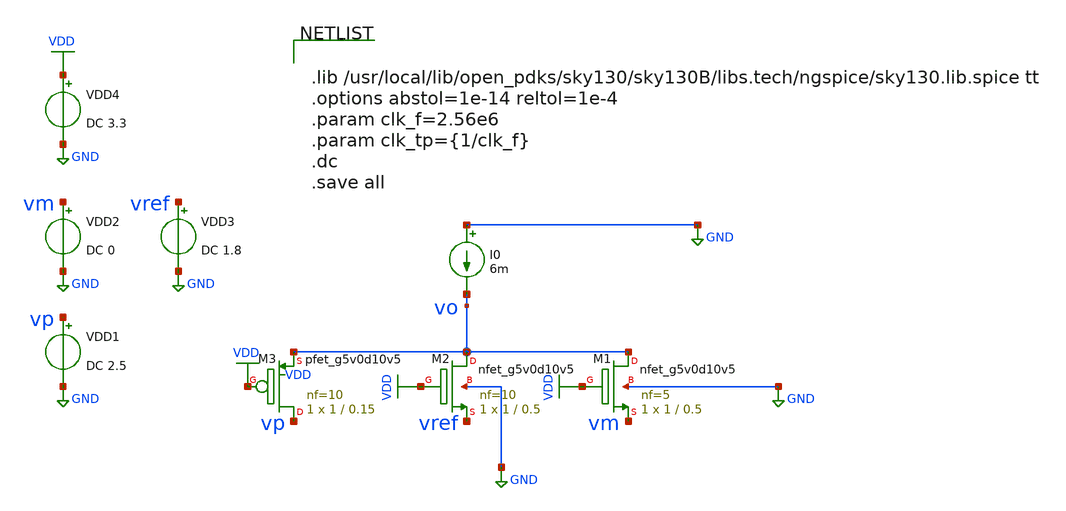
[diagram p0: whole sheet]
** sch_path: xschem/tryandtest/tb_fingers.sch
**.subckt tb_fingers
VDD4 VDD GND DC 3.3
VDD1 vp GND DC 2.5
VDD2 vm GND DC 0
VDD3 vref GND DC 1.8
I0 GND vo 6m
XM1 vo VDD vm GND sky130_fd_pr__nfet_g5v0d10v5 L=0.5 W=1 nf=5 ad='int((nf+1)/2) * W/nf * 0.29' as='int((nf+2)/2) * W/nf * 0.29'
+ pd='2*int((nf+1)/2) * (W/nf + 0.29)' ps='2*int((nf+2)/2) * (W/nf + 0.29)' nrd='0.29 / W' nrs='0.29 / W'
+ sa=0 sb=0 sd=0 mult=1 m=1
XM2 vo VDD vref GND sky130_fd_pr__nfet_g5v0d10v5 L=0.5 W=1 nf=10 ad='int((nf+1)/2) * W/nf * 0.29' as='int((nf+2)/2) * W/nf * 0.29'
+ pd='2*int((nf+1)/2) * (W/nf + 0.29)' ps='2*int((nf+2)/2) * (W/nf + 0.29)' nrd='0.29 / W' nrs='0.29 / W'
+ sa=0 sb=0 sd=0 mult=1 m=1
XM3 vp VDD vo VDD sky130_fd_pr__pfet_g5v0d10v5 L=0.15 W=1 nf=10 ad='int((nf+1)/2) * W/nf * 0.29' as='int((nf+2)/2) * W/nf * 0.29'
+ pd='2*int((nf+1)/2) * (W/nf + 0.29)' ps='2*int((nf+2)/2) * (W/nf + 0.29)' nrd='0.29 / W' nrs='0.29 / W'
+ sa=0 sb=0 sd=0 mult=1 m=1
**** begin user architecture code


.lib /usr/local/lib/open_pdks/sky130/sky130B/libs.tech/ngspice/sky130.lib.spice tt
.options abstol=1e-14 reltol=1e-4
.param clk_f=2.56e6
.param clk_tp={1/clk_f}
.dc
.save all


**** end user architecture code
**.ends
.GLOBAL GND
.GLOBAL VDD
.end
